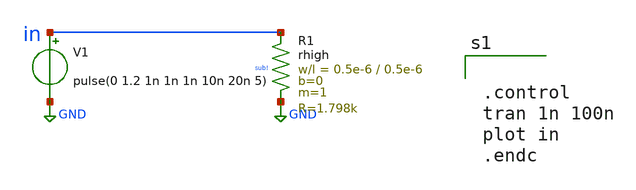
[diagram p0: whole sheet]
** sch_path: xschem/pulse.sch
**.subckt pulse
V1 in GND pulse(0 1.2 1n 1n 1n 10n 20n 5)
XR1 in GND sub! rhigh w=0.5e-6 l=0.5e-6 m=1 b=0 mm_ok=1
**** begin user architecture code


.control
tran 1n 100n
plot in
.endc


**** end user architecture code
**.ends
.GLOBAL GND
.end
